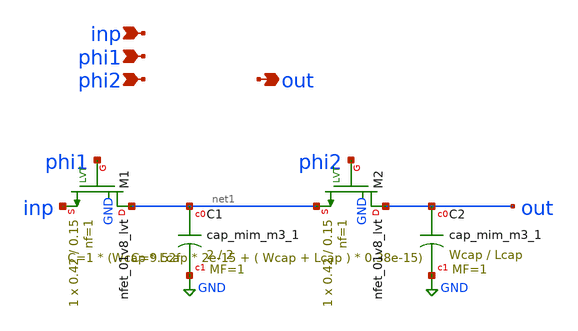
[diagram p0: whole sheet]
** sch_path: xschem/tryandtest/nmosRC.sch
**.subckt nmosRC out phi2 phi1 inp
*.opin out
*.ipin phi2
*.ipin phi1
*.ipin inp
XC1 net1 GND sky130_fd_pr__cap_mim_m3_1 W=2 L=2 MF=1 m=1
XC2 out GND sky130_fd_pr__cap_mim_m3_1 W=Wcap L=Lcap MF=1 m=1
XM1 net1 phi1 inp GND sky130_fd_pr__nfet_01v8_lvt L=0.15 W=0.42 nf=1 ad='int((nf+1)/2) * W/nf * 0.29'
+ as='int((nf+2)/2) * W/nf * 0.29' pd='2*int((nf+1)/2) * (W/nf + 0.29)' ps='2*int((nf+2)/2) * (W/nf + 0.29)'
+ nrd='0.29 / W' nrs='0.29 / W' sa=0 sb=0 sd=0 mult=1 m=1
XM2 out phi2 net1 GND sky130_fd_pr__nfet_01v8_lvt L=0.15 W=0.42 nf=1 ad='int((nf+1)/2) * W/nf * 0.29'
+ as='int((nf+2)/2) * W/nf * 0.29' pd='2*int((nf+1)/2) * (W/nf + 0.29)' ps='2*int((nf+2)/2) * (W/nf + 0.29)'
+ nrd='0.29 / W' nrs='0.29 / W' sa=0 sb=0 sd=0 mult=1 m=1
**.ends
.GLOBAL GND
.end
